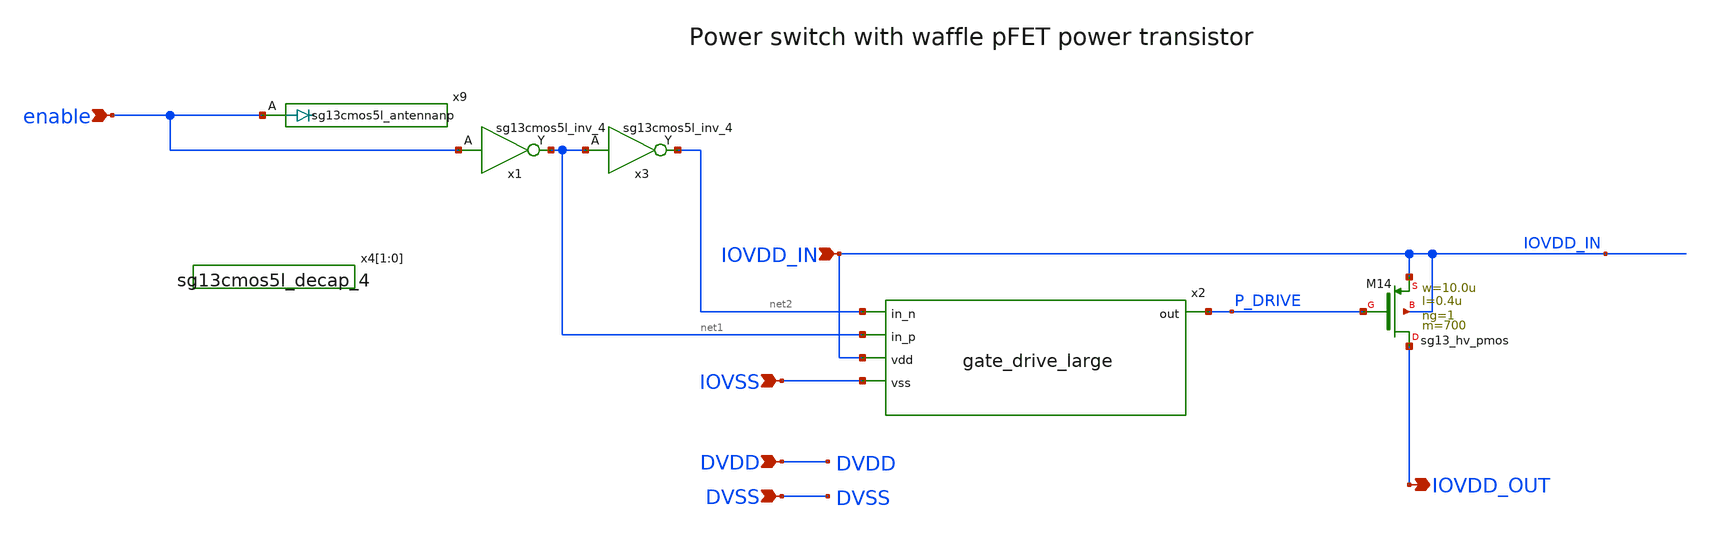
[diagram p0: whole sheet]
** sch_path: xschem/power_stage2.sch
**.subckt power_stage2 enable IOVDD_IN DVSS DVDD IOVSS IOVDD_OUT
*.ipin enable
*.ipin IOVDD_IN
*.ipin DVSS
*.ipin DVDD
*.ipin IOVSS
*.opin IOVDD_OUT
XM14 IOVDD_OUT P_DRIVE IOVDD_IN IOVDD_IN sg13_hv_pmos w=10.0u l=0.4u ng=1 m=700 mm_ok=1
x2 net2 net1 P_DRIVE IOVDD_IN IOVSS gate_drive_large
x1 net1 enable DVDD DVSS sg13cmos5l_inv_4
x3 net2 net1 DVDD DVSS sg13cmos5l_inv_4
x4[1] DVDD DVSS sg13cmos5l_decap_4
x4[0] DVDD DVSS sg13cmos5l_decap_4
x9 enable DVDD DVSS sg13cmos5l_antennanp
**.ends

* expanding   symbol:  gate_drive_large.sym # of pins=5
** sym_path: xschem/gate_drive_large.sym
** sch_path: xschem/gate_drive_large.sch
.subckt gate_drive_large in_n in_p out vdd vss
*.ipin in_n
*.ipin in_p
*.ipin vdd
*.ipin vss
*.opin out
XM1 net1 in_p vss vss sg13_hv_nmos w=2u l=0.5u ng=1 m=2 mm_ok=1
XM2 net1 S1_N vdd vdd sg13_hv_pmos w=1u l=0.5u ng=1 m=2 mm_ok=1
XM3 S1_N in_n vss vss sg13_hv_nmos w=2u l=0.5u ng=1 m=2 mm_ok=1
XM4 S1_N net1 vdd vdd sg13_hv_pmos w=1u l=0.5u ng=1 m=2 mm_ok=1
XM5 S2_N S1_N vdd vdd sg13_hv_pmos w=10u l=0.5u ng=1 m=2 mm_ok=1
XM6 S2_N S1_N vss vss sg13_hv_nmos w=5u l=0.5u ng=1 m=2 mm_ok=1
XM7 S3_N S2_N vdd vdd sg13_hv_pmos w=10u l=0.5u ng=1 m=6 mm_ok=1
XM8 S3_N S2_N vss vss sg13_hv_nmos w=5u l=0.5u ng=1 m=6 mm_ok=1
XM9 S4_N S3_N vdd vdd sg13_hv_pmos w=10u l=0.5u ng=1 m=20 mm_ok=1
XM10 S4_N S3_N vss vss sg13_hv_nmos w=5u l=0.5u ng=1 m=20 mm_ok=1
XM11 out S4_N vdd vdd sg13_hv_pmos w=10u l=0.5u ng=1 m=60 mm_ok=1
XM12 out S4_N vss vss sg13_hv_nmos w=5u l=0.5u ng=1 m=60 mm_ok=1
.ends

.end
